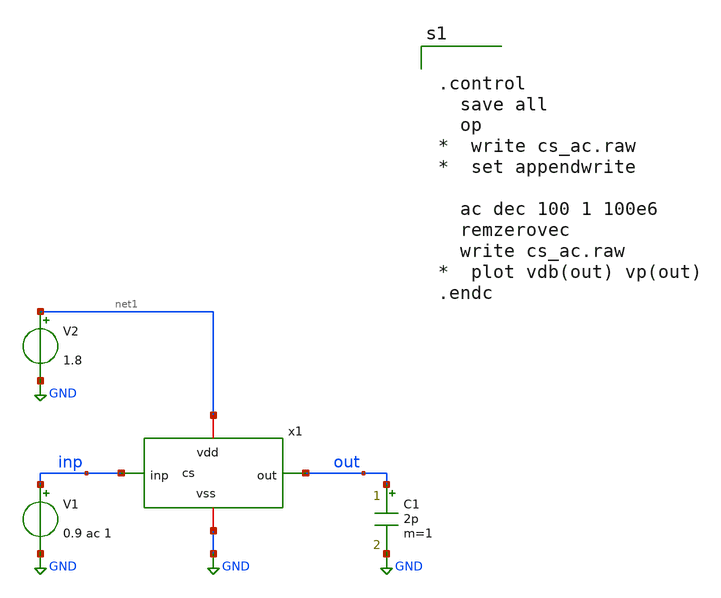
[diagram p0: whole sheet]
** sch_path: xschem/cs_ac.sch
**.subckt cs_ac
x1 out inp net1 GND cs
V1 inp GND 0.9 ac 1
V2 net1 GND 1.8
C1 out GND 2p m=1
**** begin user architecture code

** opencircuitdesign pdks install
.lib $::SKYWATER_MODELS/sky130.lib.spice tt




.control
  save all
  op
*  write cs_ac.raw
*  set appendwrite

  ac dec 100 1 100e6
  remzerovec
  write cs_ac.raw
*  plot vdb(out) vp(out)
.endc


**** end user architecture code
**.ends

* expanding   symbol:  cs.sym # of pins=4
** sym_path: xschem/cs.sym
.include cs_pex.spice
.GLOBAL GND
.end
